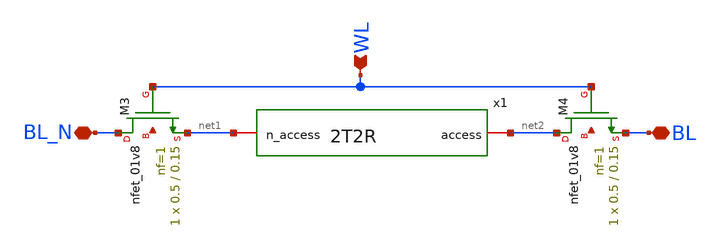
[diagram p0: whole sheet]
** sch_path: analog/schematics/Access_2T2R.sch
**.subckt Access_2T2R BL_N BL WL
*.iopin BL_N
*.iopin BL
*.ipin WL
XM3 BL_N WL net1 net3 sky130_fd_pr__nfet_01v8 L=0.15 W=0.5 nf=1 ad='int((nf+1)/2) * W/nf * 0.29' as='int((nf+2)/2) * W/nf * 0.29'
+ pd='2*int((nf+1)/2) * (W/nf + 0.29)' ps='2*int((nf+2)/2) * (W/nf + 0.29)' nrd='0.29 / W' nrs='0.29 / W'
+ sa=0 sb=0 sd=0 mult=1 m=1
XM4 net2 WL BL net4 sky130_fd_pr__nfet_01v8 L=0.15 W=0.5 nf=1 ad='int((nf+1)/2) * W/nf * 0.29' as='int((nf+2)/2) * W/nf * 0.29'
+ pd='2*int((nf+1)/2) * (W/nf + 0.29)' ps='2*int((nf+2)/2) * (W/nf + 0.29)' nrd='0.29 / W' nrs='0.29 / W'
+ sa=0 sb=0 sd=0 mult=1 m=1
x1 net1 net2 2T2R
**.ends

* expanding   symbol:  2T2R.sym # of pins=2
** sym_path: analog/schematics/2T2R.sym
** sch_path: analog/schematics/2T2R.sch
.subckt 2T2R n_access access
*.iopin access
*.iopin n_access
XM1 access n_access GND net1 sky130_fd_pr__nfet_01v8 L=0.15 W=1 nf=1 ad='int((nf+1)/2) * W/nf * 0.29'
+ as='int((nf+2)/2) * W/nf * 0.29' pd='2*int((nf+1)/2) * (W/nf + 0.29)' ps='2*int((nf+2)/2) * (W/nf + 0.29)'
+ nrd='0.29 / W' nrs='0.29 / W' sa=0 sb=0 sd=0 mult=1 m=1
XM2 n_access access GND net2 sky130_fd_pr__nfet_01v8 L=0.15 W=1 nf=1 ad='int((nf+1)/2) * W/nf * 0.29'
+ as='int((nf+2)/2) * W/nf * 0.29' pd='2*int((nf+1)/2) * (W/nf + 0.29)' ps='2*int((nf+2)/2) * (W/nf + 0.29)'
+ nrd='0.29 / W' nrs='0.29 / W' sa=0 sb=0 sd=0 mult=1 m=1
XR1 n_access VDD net3 sky130_fd_pr__res_high_po W=2 L=314 mult=1 m=1
XR2 access VDD net4 sky130_fd_pr__res_high_po W=2 L=314 mult=1 m=1
.ends

.GLOBAL VDD
.GLOBAL GND
.end
